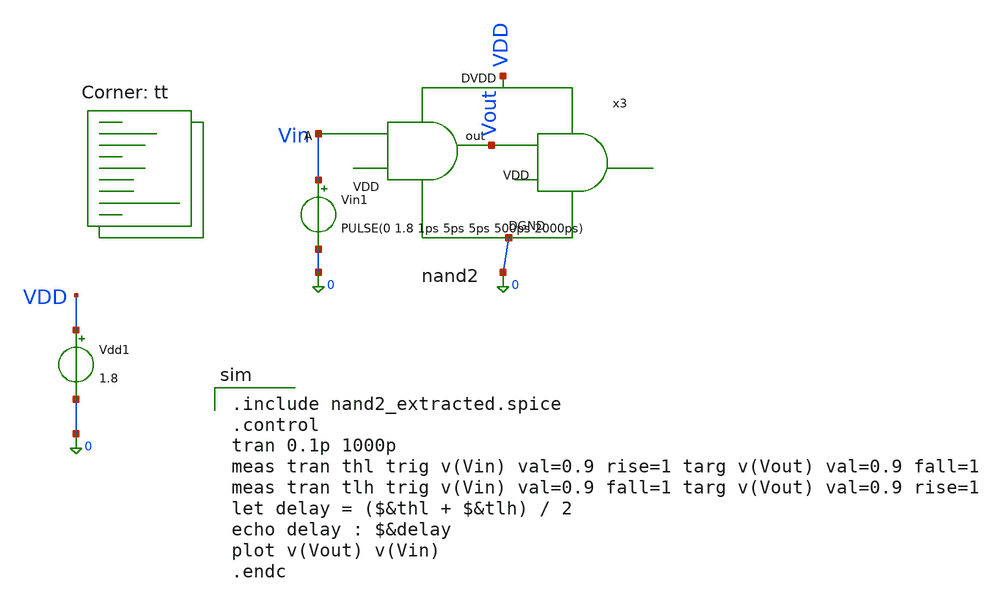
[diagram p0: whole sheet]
** sch_path: tutorial-5/source/qn_1_b.sch
**.subckt qn_1_b
Vin1 Vin 0 PULSE(0 1.8 1ps 5ps 5ps 500ps 2000ps)
Vdd1 VDD 0 1.8
x3 VDD Vout Vin 0 nand2
**** begin user architecture code

.include nand2_extracted.spice
.control
tran 0.1p 1000p
meas tran thl trig v(Vin) val=0.9 rise=1 targ v(Vout) val=0.9 fall=1
meas tran tlh trig v(Vin) val=0.9 fall=1 targ v(Vout) val=0.9 rise=1
let delay = ($&thl + $&tlh) / 2
echo delay : $&delay
plot v(Vout) v(Vin)
.endc

.lib $::SKYWATER_MODELS/sky130.lib.spice tt
**** end user architecture code
**.ends

* expanding   symbol:  nand2.sym # of pins=4
** sym_path: tutorial-5/source/nand2.sym
** sch_path: tutorial-5/source/nand2.sch
.subckt nand2 DVDD out A DGND
*.iopin DVDD
*.iopin DGND
*.iopin A
*.iopin out
XM1 DVDD A out DVDD sky130_fd_pr__pfet_01v8 L=0.15 W=1.68 nf=1 ad='int((nf+1)/2) * W/nf * 0.29' as='int((nf+2)/2) * W/nf * 0.29'
+ pd='2*int((nf+1)/2) * (W/nf + 0.29)' ps='2*int((nf+2)/2) * (W/nf + 0.29)' nrd='0.29 / W' nrs='0.29 / W'
+ sa=0 sb=0 sd=0 mult=1 m=1
XM2 out DVDD DVDD DVDD sky130_fd_pr__pfet_01v8 L=0.15 W=1.68 nf=1 ad='int((nf+1)/2) * W/nf * 0.29' as='int((nf+2)/2) * W/nf * 0.29'
+ pd='2*int((nf+1)/2) * (W/nf + 0.29)' ps='2*int((nf+2)/2) * (W/nf + 0.29)' nrd='0.29 / W' nrs='0.29 / W'
+ sa=0 sb=0 sd=0 mult=1 m=1
XM3 out DVDD net1 DGND sky130_fd_pr__nfet_01v8 L=0.15 W=1.68 nf=1 ad='int((nf+1)/2) * W/nf * 0.29' as='int((nf+2)/2) * W/nf * 0.29'
+ pd='2*int((nf+1)/2) * (W/nf + 0.29)' ps='2*int((nf+2)/2) * (W/nf + 0.29)' nrd='0.29 / W' nrs='0.29 / W'
+ sa=0 sb=0 sd=0 mult=1 m=1
XM4 DGND A net1 DGND sky130_fd_pr__nfet_01v8 L=0.15 W=1.68 nf=1 ad='int((nf+1)/2) * W/nf * 0.29' as='int((nf+2)/2) * W/nf * 0.29'
+ pd='2*int((nf+1)/2) * (W/nf + 0.29)' ps='2*int((nf+2)/2) * (W/nf + 0.29)' nrd='0.29 / W' nrs='0.29 / W'
+ sa=0 sb=0 sd=0 mult=1 m=1
XM5 DVDD out net2 DVDD sky130_fd_pr__pfet_01v8 L=0.15 W=1.68 nf=1 ad='int((nf+1)/2) * W/nf * 0.29' as='int((nf+2)/2) * W/nf * 0.29'
+ pd='2*int((nf+1)/2) * (W/nf + 0.29)' ps='2*int((nf+2)/2) * (W/nf + 0.29)' nrd='0.29 / W' nrs='0.29 / W'
+ sa=0 sb=0 sd=0 mult=1 m=1
XM6 net2 DVDD DVDD DVDD sky130_fd_pr__pfet_01v8 L=0.15 W=1.68 nf=1 ad='int((nf+1)/2) * W/nf * 0.29' as='int((nf+2)/2) * W/nf * 0.29'
+ pd='2*int((nf+1)/2) * (W/nf + 0.29)' ps='2*int((nf+2)/2) * (W/nf + 0.29)' nrd='0.29 / W' nrs='0.29 / W'
+ sa=0 sb=0 sd=0 mult=1 m=1
XM7 net2 DVDD net3 DGND sky130_fd_pr__nfet_01v8 L=0.15 W=1.68 nf=1 ad='int((nf+1)/2) * W/nf * 0.29' as='int((nf+2)/2) * W/nf * 0.29'
+ pd='2*int((nf+1)/2) * (W/nf + 0.29)' ps='2*int((nf+2)/2) * (W/nf + 0.29)' nrd='0.29 / W' nrs='0.29 / W'
+ sa=0 sb=0 sd=0 mult=1 m=1
XM8 DGND out net3 DGND sky130_fd_pr__nfet_01v8 L=0.15 W=1.68 nf=1 ad='int((nf+1)/2) * W/nf * 0.29' as='int((nf+2)/2) * W/nf * 0.29'
+ pd='2*int((nf+1)/2) * (W/nf + 0.29)' ps='2*int((nf+2)/2) * (W/nf + 0.29)' nrd='0.29 / W' nrs='0.29 / W'
+ sa=0 sb=0 sd=0 mult=1 m=1
.ends

.end
